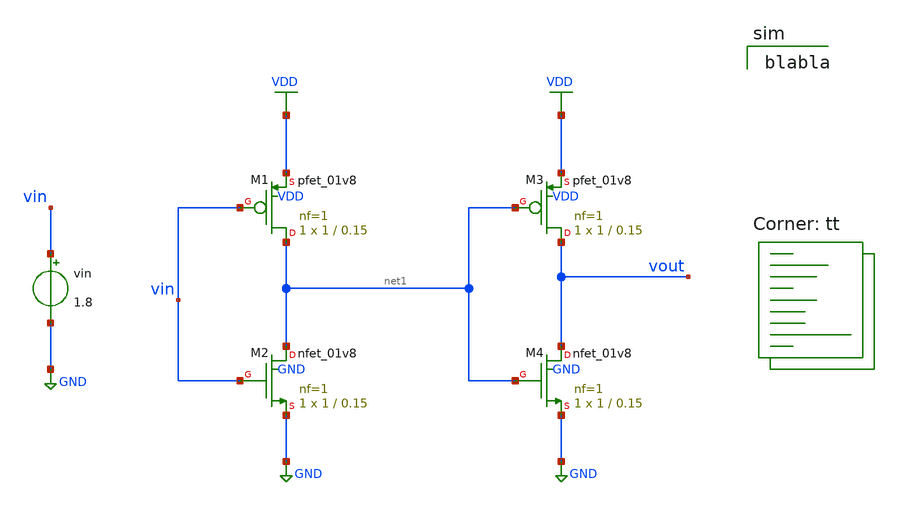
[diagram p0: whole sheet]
** sch_path: assignments/assignment3/assign1b.sch
**.subckt assign1b
XM1 net1 vin VDD VDD sky130_fd_pr__pfet_01v8 L=0.15 W=1 nf=1 ad='int((nf+1)/2) * W/nf * 0.29' as='int((nf+2)/2) * W/nf * 0.29'
+ pd='2*int((nf+1)/2) * (W/nf + 0.29)' ps='2*int((nf+2)/2) * (W/nf + 0.29)' nrd='0.29 / W' nrs='0.29 / W'
+ sa=0 sb=0 sd=0 mult=1 m=1
XM2 net1 vin GND GND sky130_fd_pr__nfet_01v8 L=0.15 W=1 nf=1 ad='int((nf+1)/2) * W/nf * 0.29' as='int((nf+2)/2) * W/nf * 0.29'
+ pd='2*int((nf+1)/2) * (W/nf + 0.29)' ps='2*int((nf+2)/2) * (W/nf + 0.29)' nrd='0.29 / W' nrs='0.29 / W'
+ sa=0 sb=0 sd=0 mult=1 m=1
XM3 vout net1 VDD VDD sky130_fd_pr__pfet_01v8 L=0.15 W=1 nf=1 ad='int((nf+1)/2) * W/nf * 0.29' as='int((nf+2)/2) * W/nf * 0.29'
+ pd='2*int((nf+1)/2) * (W/nf + 0.29)' ps='2*int((nf+2)/2) * (W/nf + 0.29)' nrd='0.29 / W' nrs='0.29 / W'
+ sa=0 sb=0 sd=0 mult=1 m=1
XM4 vout net1 GND GND sky130_fd_pr__nfet_01v8 L=0.15 W=1 nf=1 ad='int((nf+1)/2) * W/nf * 0.29' as='int((nf+2)/2) * W/nf * 0.29'
+ pd='2*int((nf+1)/2) * (W/nf + 0.29)' ps='2*int((nf+2)/2) * (W/nf + 0.29)' nrd='0.29 / W' nrs='0.29 / W'
+ sa=0 sb=0 sd=0 mult=1 m=1
vin vin GND 1.8
**** begin user architecture code

blabla

.lib $::SKYWATER_MODELS/sky130.lib.spice tt
**** end user architecture code
**.ends
.GLOBAL VDD
.GLOBAL GND
.end
